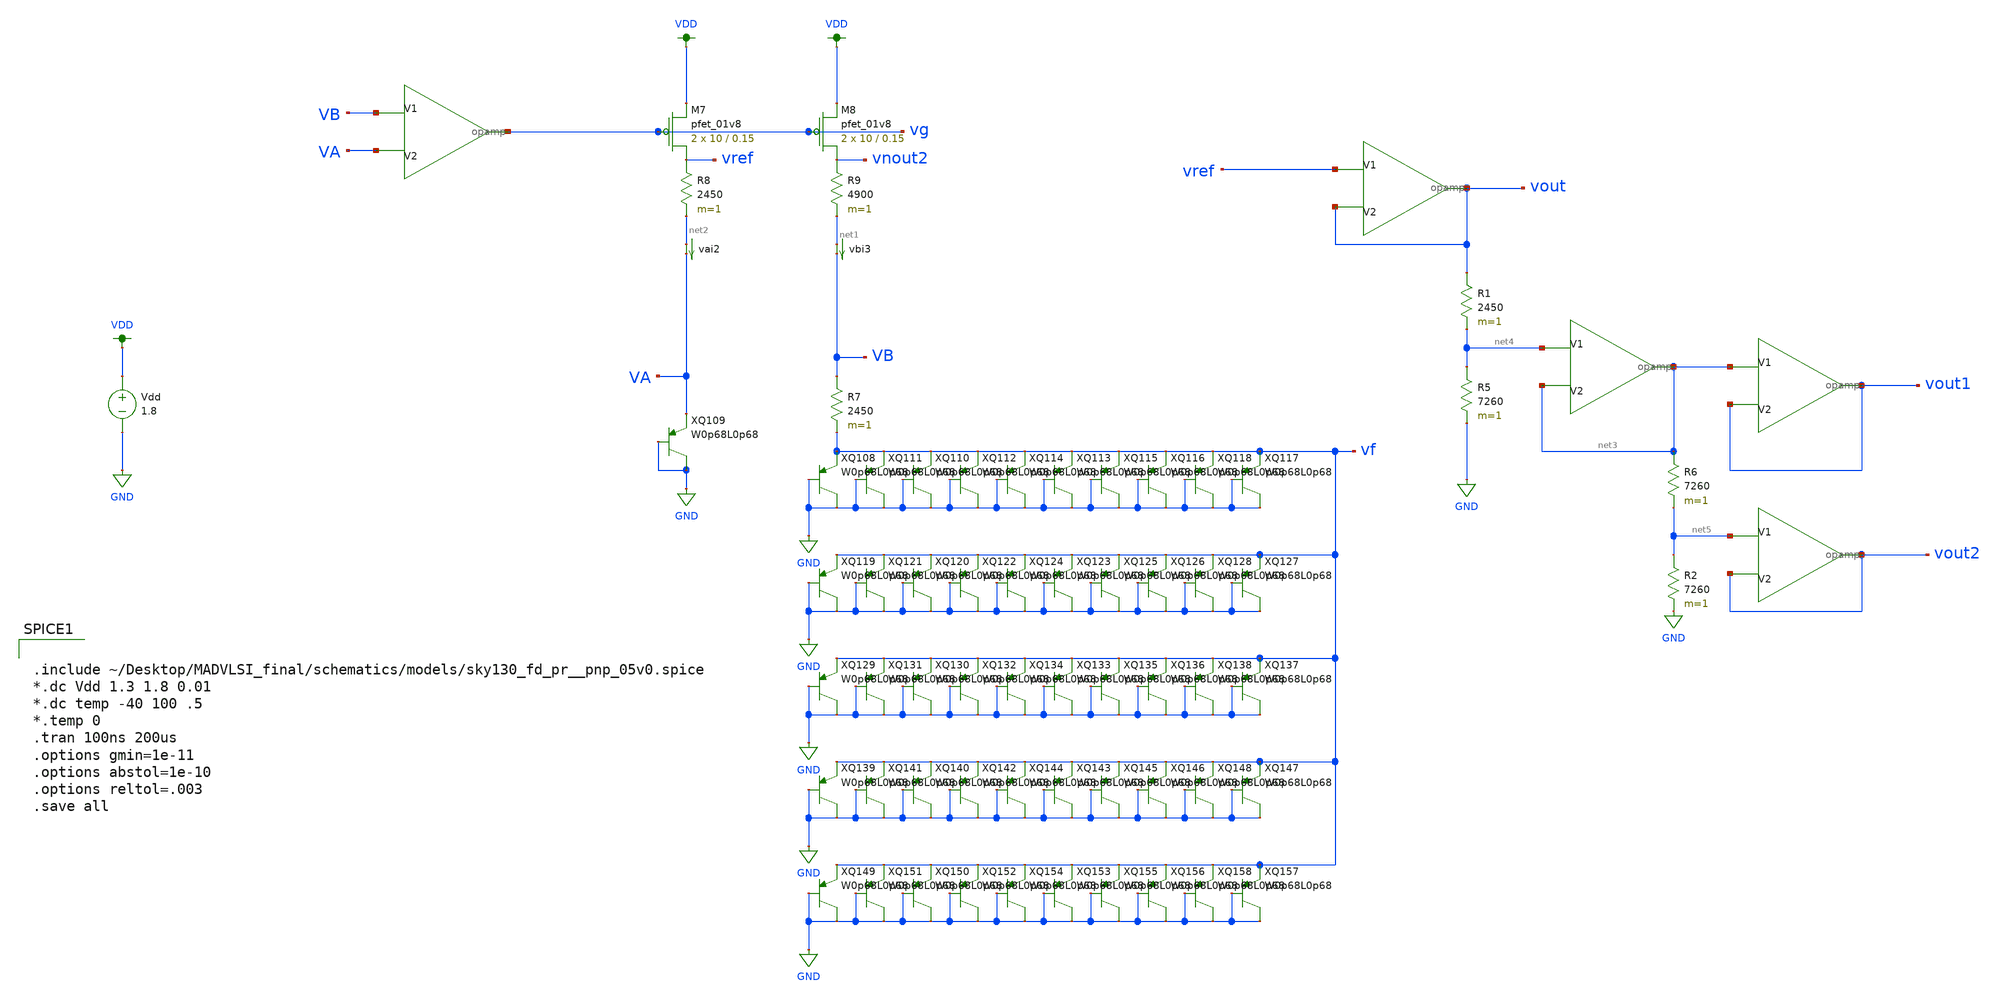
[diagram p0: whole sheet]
** sch_path: schematics/bandgap.sch
**.subckt bandgap
Vdd VDD GND 1.8
XM7 vref vg VDD VDD sky130_fd_pr__pfet_01v8 L=0.15 W=10 nf=1 ad='int((nf+1)/2) * W/nf * 0.29' as='int((nf+2)/2) * W/nf * 0.29'
+ pd='2*int((nf+1)/2) * (W/nf + 0.29)' ps='2*int((nf+2)/2) * (W/nf + 0.29)' nrd='0.29 / W' nrs='0.29 / W'
+ sa=0 sb=0 sd=0 mult=2 m=2
XQ108 vf GND GND sky130_fd_pr__pnp_05v0
XQ109 VA GND GND sky130_fd_pr__pnp_05v0
R7 VB vf 2450 m=1
XQ110 vf GND GND sky130_fd_pr__pnp_05v0
XQ111 vf GND GND sky130_fd_pr__pnp_05v0
XQ112 vf GND GND sky130_fd_pr__pnp_05v0
XQ113 vf GND GND sky130_fd_pr__pnp_05v0
XQ114 vf GND GND sky130_fd_pr__pnp_05v0
XQ115 vf GND GND sky130_fd_pr__pnp_05v0
XQ116 vf GND GND sky130_fd_pr__pnp_05v0
XQ117 vf GND GND sky130_fd_pr__pnp_05v0
XQ118 vf GND GND sky130_fd_pr__pnp_05v0
XQ119 vf GND GND sky130_fd_pr__pnp_05v0
XQ120 vf GND GND sky130_fd_pr__pnp_05v0
XQ121 vf GND GND sky130_fd_pr__pnp_05v0
XQ122 vf GND GND sky130_fd_pr__pnp_05v0
XQ123 vf GND GND sky130_fd_pr__pnp_05v0
XQ124 vf GND GND sky130_fd_pr__pnp_05v0
XQ125 vf GND GND sky130_fd_pr__pnp_05v0
XQ126 vf GND GND sky130_fd_pr__pnp_05v0
XQ127 vf GND GND sky130_fd_pr__pnp_05v0
XQ128 vf GND GND sky130_fd_pr__pnp_05v0
XQ129 vf GND GND sky130_fd_pr__pnp_05v0
XQ130 vf GND GND sky130_fd_pr__pnp_05v0
XQ131 vf GND GND sky130_fd_pr__pnp_05v0
XQ132 vf GND GND sky130_fd_pr__pnp_05v0
XQ133 vf GND GND sky130_fd_pr__pnp_05v0
XQ134 vf GND GND sky130_fd_pr__pnp_05v0
XQ135 vf GND GND sky130_fd_pr__pnp_05v0
XQ136 vf GND GND sky130_fd_pr__pnp_05v0
XQ137 vf GND GND sky130_fd_pr__pnp_05v0
XQ138 vf GND GND sky130_fd_pr__pnp_05v0
XQ139 vf GND GND sky130_fd_pr__pnp_05v0
XQ140 vf GND GND sky130_fd_pr__pnp_05v0
XQ141 vf GND GND sky130_fd_pr__pnp_05v0
XQ142 vf GND GND sky130_fd_pr__pnp_05v0
XQ143 vf GND GND sky130_fd_pr__pnp_05v0
XQ144 vf GND GND sky130_fd_pr__pnp_05v0
XQ145 vf GND GND sky130_fd_pr__pnp_05v0
XQ146 vf GND GND sky130_fd_pr__pnp_05v0
XQ147 vf GND GND sky130_fd_pr__pnp_05v0
XQ148 vf GND GND sky130_fd_pr__pnp_05v0
XQ149 vf GND GND sky130_fd_pr__pnp_05v0
XQ150 vf GND GND sky130_fd_pr__pnp_05v0
XQ151 vf GND GND sky130_fd_pr__pnp_05v0
XQ152 vf GND GND sky130_fd_pr__pnp_05v0
XQ153 vf GND GND sky130_fd_pr__pnp_05v0
XQ154 vf GND GND sky130_fd_pr__pnp_05v0
XQ155 vf GND GND sky130_fd_pr__pnp_05v0
XQ156 vf GND GND sky130_fd_pr__pnp_05v0
XQ157 vf GND GND sky130_fd_pr__pnp_05v0
XQ158 vf GND GND sky130_fd_pr__pnp_05v0
vai2 net2 VA 0
.save i(vai2)
vbi3 net1 VB 0
.save i(vbi3)
X159 VB VA vg opamp
R8 vref net2 2450 m=1
R9 vnout2 net1 4900 m=1
XM8 vnout2 vg VDD VDD sky130_fd_pr__pfet_01v8 L=0.15 W=10 nf=1 ad='int((nf+1)/2) * W/nf * 0.29' as='int((nf+2)/2) * W/nf * 0.29'
+ pd='2*int((nf+1)/2) * (W/nf + 0.29)' ps='2*int((nf+2)/2) * (W/nf + 0.29)' nrd='0.29 / W' nrs='0.29 / W'
+ sa=0 sb=0 sd=0 mult=2 m=2
X2 vref vout vout opamp
R1 vout net4 2450 m=1
R5 net4 GND 7260 m=1
X3 net4 net3 net3 opamp
R6 net3 net5 7260 m=1
R2 net5 GND 7260 m=1
X4 net5 vout2 vout2 opamp
X5 net3 vout1 vout1 opamp
**** begin user architecture code

.option wnflag=1
.param MC_SWITCH=0.0
.lib ~/skywater/skywater-pdk/libraries/sky130_fd_pr_ngspice/latest/models/sky130.lib.spice tt



.include ~/Desktop/MADVLSI_final/schematics/models/sky130_fd_pr__pnp_05v0.spice
*.dc Vdd 1.3 1.8 0.01
*.dc temp -40 100 .5
*.temp 0
.tran 100ns 200us
.options gmin=1e-11
.options abstol=1e-10
.options reltol=.003
.save all


**** end user architecture code
**.ends

* expanding   symbol:  /home/madvlsi/Desktop/MADVLSI_final/schematics/opamp.sym # of pins=3
** sym_path: schematics/opamp.sym
** sch_path: schematics/opamp.sch
.subckt opamp V1 V2 VOUT
*.ipin V1
*.ipin V2
*.opin VOUT
XM19 net12 net10 GND VDD sky130_fd_pr__pfet_01v8 L=.6 W=1.5 nf=1 ad='int((nf+1)/2) * W/nf * 0.29' as='int((nf+2)/2) * W/nf * 0.29'
+ pd='2*int((nf+1)/2) * (W/nf + 0.29)' ps='2*int((nf+2)/2) * (W/nf + 0.29)' nrd='0.29 / W' nrs='0.29 / W'
+ sa=0 sb=0 sd=0 mult=1 m=1
XMD20 VDD VDD net12 VDD sky130_fd_pr__pfet_01v8 L=.6 W=1.5 nf=1 ad='int((nf+1)/2) * W/nf * 0.29' as='int((nf+2)/2) * W/nf * 0.29'
+ pd='2*int((nf+1)/2) * (W/nf + 0.29)' ps='2*int((nf+2)/2) * (W/nf + 0.29)' nrd='0.29 / W' nrs='0.29 / W'
+ sa=0 sb=0 sd=0 mult=1 m=1
XM22 net12 net10 net9 VDD sky130_fd_pr__pfet_01v8 L=.6 W=1.5 nf=1 ad='int((nf+1)/2) * W/nf * 0.29' as='int((nf+2)/2) * W/nf * 0.29'
+ pd='2*int((nf+1)/2) * (W/nf + 0.29)' ps='2*int((nf+2)/2) * (W/nf + 0.29)' nrd='0.29 / W' nrs='0.29 / W'
+ sa=0 sb=0 sd=0 mult=1 m=1
XM23 GND net10 net12 VDD sky130_fd_pr__pfet_01v8 L=.6 W=1.5 nf=1 ad='int((nf+1)/2) * W/nf * 0.29' as='int((nf+2)/2) * W/nf * 0.29'
+ pd='2*int((nf+1)/2) * (W/nf + 0.29)' ps='2*int((nf+2)/2) * (W/nf + 0.29)' nrd='0.29 / W' nrs='0.29 / W'
+ sa=0 sb=0 sd=0 mult=1 m=1
XMD24 net9 VDD net10 VDD sky130_fd_pr__pfet_01v8 L=.6 W=1.5 nf=1 ad='int((nf+1)/2) * W/nf * 0.29' as='int((nf+2)/2) * W/nf * 0.29'
+ pd='2*int((nf+1)/2) * (W/nf + 0.29)' ps='2*int((nf+2)/2) * (W/nf + 0.29)' nrd='0.29 / W' nrs='0.29 / W'
+ sa=0 sb=0 sd=0 mult=1 m=1
XM25 VDD net10 net12 VDD sky130_fd_pr__pfet_01v8 L=.6 W=1.5 nf=1 ad='int((nf+1)/2) * W/nf * 0.29' as='int((nf+2)/2) * W/nf * 0.29'
+ pd='2*int((nf+1)/2) * (W/nf + 0.29)' ps='2*int((nf+2)/2) * (W/nf + 0.29)' nrd='0.29 / W' nrs='0.29 / W'
+ sa=0 sb=0 sd=0 mult=1 m=1
XM26 net7 V2 net11 VDD sky130_fd_pr__pfet_01v8 L=.6 W=1.5 nf=1 ad='int((nf+1)/2) * W/nf * 0.29' as='int((nf+2)/2) * W/nf * 0.29'
+ pd='2*int((nf+1)/2) * (W/nf + 0.29)' ps='2*int((nf+2)/2) * (W/nf + 0.29)' nrd='0.29 / W' nrs='0.29 / W'
+ sa=0 sb=0 sd=0 mult=1 m=1
XMD27 net5 VDD net14 VDD sky130_fd_pr__pfet_01v8 L=.6 W=1.5 nf=1 ad='int((nf+1)/2) * W/nf * 0.29' as='int((nf+2)/2) * W/nf * 0.29'
+ pd='2*int((nf+1)/2) * (W/nf + 0.29)' ps='2*int((nf+2)/2) * (W/nf + 0.29)' nrd='0.29 / W' nrs='0.29 / W'
+ sa=0 sb=0 sd=0 mult=1 m=1
XM28 net6 V1 net11 VDD sky130_fd_pr__pfet_01v8 L=.6 W=1.5 nf=1 ad='int((nf+1)/2) * W/nf * 0.29' as='int((nf+2)/2) * W/nf * 0.29'
+ pd='2*int((nf+1)/2) * (W/nf + 0.29)' ps='2*int((nf+2)/2) * (W/nf + 0.29)' nrd='0.29 / W' nrs='0.29 / W'
+ sa=0 sb=0 sd=0 mult=1 m=1
XM29 net11 net10 VDD VDD sky130_fd_pr__pfet_01v8 L=.6 W=1.5 nf=1 ad='int((nf+1)/2) * W/nf * 0.29' as='int((nf+2)/2) * W/nf * 0.29'
+ pd='2*int((nf+1)/2) * (W/nf + 0.29)' ps='2*int((nf+2)/2) * (W/nf + 0.29)' nrd='0.29 / W' nrs='0.29 / W'
+ sa=0 sb=0 sd=0 mult=1 m=1
XMD30 net11 VDD VDD VDD sky130_fd_pr__pfet_01v8 L=.6 W=1.5 nf=1 ad='int((nf+1)/2) * W/nf * 0.29' as='int((nf+2)/2) * W/nf * 0.29'
+ pd='2*int((nf+1)/2) * (W/nf + 0.29)' ps='2*int((nf+2)/2) * (W/nf + 0.29)' nrd='0.29 / W' nrs='0.29 / W'
+ sa=0 sb=0 sd=0 mult=1 m=1
XMD31 net2 VDD net13 VDD sky130_fd_pr__pfet_01v8 L=.6 W=1.5 nf=1 ad='int((nf+1)/2) * W/nf * 0.29' as='int((nf+2)/2) * W/nf * 0.29'
+ pd='2*int((nf+1)/2) * (W/nf + 0.29)' ps='2*int((nf+2)/2) * (W/nf + 0.29)' nrd='0.29 / W' nrs='0.29 / W'
+ sa=0 sb=0 sd=0 mult=1 m=1
XM32 net4 net5 net5 VDD sky130_fd_pr__pfet_01v8 L=.6 W=1.5 nf=1 ad='int((nf+1)/2) * W/nf * 0.29' as='int((nf+2)/2) * W/nf * 0.29'
+ pd='2*int((nf+1)/2) * (W/nf + 0.29)' ps='2*int((nf+2)/2) * (W/nf + 0.29)' nrd='0.29 / W' nrs='0.29 / W'
+ sa=0 sb=0 sd=0 mult=1 m=1
XM33 VDD net10 net4 VDD sky130_fd_pr__pfet_01v8 L=.6 W=1.5 nf=1 ad='int((nf+1)/2) * W/nf * 0.29' as='int((nf+2)/2) * W/nf * 0.29'
+ pd='2*int((nf+1)/2) * (W/nf + 0.29)' ps='2*int((nf+2)/2) * (W/nf + 0.29)' nrd='0.29 / W' nrs='0.29 / W'
+ sa=0 sb=0 sd=0 mult=1 m=1
XM34 net3 net5 net2 VDD sky130_fd_pr__pfet_01v8 L=.6 W=1.5 nf=1 ad='int((nf+1)/2) * W/nf * 0.29' as='int((nf+2)/2) * W/nf * 0.29'
+ pd='2*int((nf+1)/2) * (W/nf + 0.29)' ps='2*int((nf+2)/2) * (W/nf + 0.29)' nrd='0.29 / W' nrs='0.29 / W'
+ sa=0 sb=0 sd=0 mult=1 m=1
XM35 VDD net10 net3 VDD sky130_fd_pr__pfet_01v8 L=.6 W=1.5 nf=1 ad='int((nf+1)/2) * W/nf * 0.29' as='int((nf+2)/2) * W/nf * 0.29'
+ pd='2*int((nf+1)/2) * (W/nf + 0.29)' ps='2*int((nf+2)/2) * (W/nf + 0.29)' nrd='0.29 / W' nrs='0.29 / W'
+ sa=0 sb=0 sd=0 mult=1 m=1
XM36 VOUT net2 VDD VDD sky130_fd_pr__pfet_01v8 L=.6 W=1.5 nf=1 ad='int((nf+1)/2) * W/nf * 0.29' as='int((nf+2)/2) * W/nf * 0.29'
+ pd='2*int((nf+1)/2) * (W/nf + 0.29)' ps='2*int((nf+2)/2) * (W/nf + 0.29)' nrd='0.29 / W' nrs='0.29 / W'
+ sa=0 sb=0 sd=0 mult=1 m=1
XM37 VDD net2 VOUT VDD sky130_fd_pr__pfet_01v8 L=.6 W=1.5 nf=1 ad='int((nf+1)/2) * W/nf * 0.29' as='int((nf+2)/2) * W/nf * 0.29'
+ pd='2*int((nf+1)/2) * (W/nf + 0.29)' ps='2*int((nf+2)/2) * (W/nf + 0.29)' nrd='0.29 / W' nrs='0.29 / W'
+ sa=0 sb=0 sd=0 mult=1 m=1
XM38 VOUT net2 VDD VDD sky130_fd_pr__pfet_01v8 L=.6 W=1.5 nf=1 ad='int((nf+1)/2) * W/nf * 0.29' as='int((nf+2)/2) * W/nf * 0.29'
+ pd='2*int((nf+1)/2) * (W/nf + 0.29)' ps='2*int((nf+2)/2) * (W/nf + 0.29)' nrd='0.29 / W' nrs='0.29 / W'
+ sa=0 sb=0 sd=0 mult=1 m=1
XM39 VDD net2 VOUT VDD sky130_fd_pr__pfet_01v8 L=.6 W=1.5 nf=1 ad='int((nf+1)/2) * W/nf * 0.29' as='int((nf+2)/2) * W/nf * 0.29'
+ pd='2*int((nf+1)/2) * (W/nf + 0.29)' ps='2*int((nf+2)/2) * (W/nf + 0.29)' nrd='0.29 / W' nrs='0.29 / W'
+ sa=0 sb=0 sd=0 mult=1 m=1
XM40 net1 net9 VDD GND sky130_fd_pr__nfet_01v8 L=.6 W=1.5 nf=1 ad='int((nf+1)/2) * W/nf * 0.29' as='int((nf+2)/2) * W/nf * 0.29'
+ pd='2*int((nf+1)/2) * (W/nf + 0.29)' ps='2*int((nf+2)/2) * (W/nf + 0.29)' nrd='0.29 / W' nrs='0.29 / W'
+ sa=0 sb=0 sd=0 mult=1 m=1
XMD41 GND GND net1 GND sky130_fd_pr__nfet_01v8 L=.6 W=1.5 nf=1 ad='int((nf+1)/2) * W/nf * 0.29' as='int((nf+2)/2) * W/nf * 0.29'
+ pd='2*int((nf+1)/2) * (W/nf + 0.29)' ps='2*int((nf+2)/2) * (W/nf + 0.29)' nrd='0.29 / W' nrs='0.29 / W'
+ sa=0 sb=0 sd=0 mult=1 m=1
XM42 net1 net9 net10 GND sky130_fd_pr__nfet_01v8 L=.6 W=1.5 nf=1 ad='int((nf+1)/2) * W/nf * 0.29' as='int((nf+2)/2) * W/nf * 0.29'
+ pd='2*int((nf+1)/2) * (W/nf + 0.29)' ps='2*int((nf+2)/2) * (W/nf + 0.29)' nrd='0.29 / W' nrs='0.29 / W'
+ sa=0 sb=0 sd=0 mult=1 m=1
XM43 VDD net9 net1 GND sky130_fd_pr__nfet_01v8 L=.6 W=1.5 nf=1 ad='int((nf+1)/2) * W/nf * 0.29' as='int((nf+2)/2) * W/nf * 0.29'
+ pd='2*int((nf+1)/2) * (W/nf + 0.29)' ps='2*int((nf+2)/2) * (W/nf + 0.29)' nrd='0.29 / W' nrs='0.29 / W'
+ sa=0 sb=0 sd=0 mult=1 m=1
XMD44 net10 GND net9 GND sky130_fd_pr__nfet_01v8 L=.6 W=1.5 nf=1 ad='int((nf+1)/2) * W/nf * 0.29' as='int((nf+2)/2) * W/nf * 0.29'
+ pd='2*int((nf+1)/2) * (W/nf + 0.29)' ps='2*int((nf+2)/2) * (W/nf + 0.29)' nrd='0.29 / W' nrs='0.29 / W'
+ sa=0 sb=0 sd=0 mult=1 m=1
XM45 GND net9 net1 GND sky130_fd_pr__nfet_01v8 L=.6 W=1.5 nf=1 ad='int((nf+1)/2) * W/nf * 0.29' as='int((nf+2)/2) * W/nf * 0.29'
+ pd='2*int((nf+1)/2) * (W/nf + 0.29)' ps='2*int((nf+2)/2) * (W/nf + 0.29)' nrd='0.29 / W' nrs='0.29 / W'
+ sa=0 sb=0 sd=0 mult=1 m=1
XM46 net3 V1 net8 GND sky130_fd_pr__nfet_01v8 L=.6 W=1.5 nf=1 ad='int((nf+1)/2) * W/nf * 0.29' as='int((nf+2)/2) * W/nf * 0.29'
+ pd='2*int((nf+1)/2) * (W/nf + 0.29)' ps='2*int((nf+2)/2) * (W/nf + 0.29)' nrd='0.29 / W' nrs='0.29 / W'
+ sa=0 sb=0 sd=0 mult=1 m=1
XMD47 net5 GND net15 GND sky130_fd_pr__nfet_01v8 L=.6 W=1.5 nf=1 ad='int((nf+1)/2) * W/nf * 0.29' as='int((nf+2)/2) * W/nf * 0.29'
+ pd='2*int((nf+1)/2) * (W/nf + 0.29)' ps='2*int((nf+2)/2) * (W/nf + 0.29)' nrd='0.29 / W' nrs='0.29 / W'
+ sa=0 sb=0 sd=0 mult=1 m=1
XM48 net4 V2 net8 GND sky130_fd_pr__nfet_01v8 L=.6 W=1.5 nf=1 ad='int((nf+1)/2) * W/nf * 0.29' as='int((nf+2)/2) * W/nf * 0.29'
+ pd='2*int((nf+1)/2) * (W/nf + 0.29)' ps='2*int((nf+2)/2) * (W/nf + 0.29)' nrd='0.29 / W' nrs='0.29 / W'
+ sa=0 sb=0 sd=0 mult=1 m=1
XM49 net8 net9 GND GND sky130_fd_pr__nfet_01v8 L=.6 W=1.5 nf=1 ad='int((nf+1)/2) * W/nf * 0.29' as='int((nf+2)/2) * W/nf * 0.29'
+ pd='2*int((nf+1)/2) * (W/nf + 0.29)' ps='2*int((nf+2)/2) * (W/nf + 0.29)' nrd='0.29 / W' nrs='0.29 / W'
+ sa=0 sb=0 sd=0 mult=1 m=1
XMD50 net8 GND GND GND sky130_fd_pr__nfet_01v8 L=.6 W=1.5 nf=1 ad='int((nf+1)/2) * W/nf * 0.29' as='int((nf+2)/2) * W/nf * 0.29'
+ pd='2*int((nf+1)/2) * (W/nf + 0.29)' ps='2*int((nf+2)/2) * (W/nf + 0.29)' nrd='0.29 / W' nrs='0.29 / W'
+ sa=0 sb=0 sd=0 mult=1 m=1
XMD51 net2 GND net16 GND sky130_fd_pr__nfet_01v8 L=.6 W=1.5 nf=1 ad='int((nf+1)/2) * W/nf * 0.29' as='int((nf+2)/2) * W/nf * 0.29'
+ pd='2*int((nf+1)/2) * (W/nf + 0.29)' ps='2*int((nf+2)/2) * (W/nf + 0.29)' nrd='0.29 / W' nrs='0.29 / W'
+ sa=0 sb=0 sd=0 mult=1 m=1
XM52 GND net9 net7 GND sky130_fd_pr__nfet_01v8 L=.6 W=1.5 nf=1 ad='int((nf+1)/2) * W/nf * 0.29' as='int((nf+2)/2) * W/nf * 0.29'
+ pd='2*int((nf+1)/2) * (W/nf + 0.29)' ps='2*int((nf+2)/2) * (W/nf + 0.29)' nrd='0.29 / W' nrs='0.29 / W'
+ sa=0 sb=0 sd=0 mult=1 m=1
XMD53 VOUT GND GND GND sky130_fd_pr__nfet_01v8 L=.6 W=1.5 nf=1 ad='int((nf+1)/2) * W/nf * 0.29' as='int((nf+2)/2) * W/nf * 0.29'
+ pd='2*int((nf+1)/2) * (W/nf + 0.29)' ps='2*int((nf+2)/2) * (W/nf + 0.29)' nrd='0.29 / W' nrs='0.29 / W'
+ sa=0 sb=0 sd=0 mult=1 m=1
XM54 GND net9 net6 GND sky130_fd_pr__nfet_01v8 L=.6 W=1.5 nf=1 ad='int((nf+1)/2) * W/nf * 0.29' as='int((nf+2)/2) * W/nf * 0.29'
+ pd='2*int((nf+1)/2) * (W/nf + 0.29)' ps='2*int((nf+2)/2) * (W/nf + 0.29)' nrd='0.29 / W' nrs='0.29 / W'
+ sa=0 sb=0 sd=0 mult=1 m=1
XM55 net7 net5 net5 GND sky130_fd_pr__nfet_01v8 L=.6 W=1.5 nf=1 ad='int((nf+1)/2) * W/nf * 0.29' as='int((nf+2)/2) * W/nf * 0.29'
+ pd='2*int((nf+1)/2) * (W/nf + 0.29)' ps='2*int((nf+2)/2) * (W/nf + 0.29)' nrd='0.29 / W' nrs='0.29 / W'
+ sa=0 sb=0 sd=0 mult=1 m=1
XM56 net6 net5 net2 GND sky130_fd_pr__nfet_01v8 L=.6 W=1.5 nf=1 ad='int((nf+1)/2) * W/nf * 0.29' as='int((nf+2)/2) * W/nf * 0.29'
+ pd='2*int((nf+1)/2) * (W/nf + 0.29)' ps='2*int((nf+2)/2) * (W/nf + 0.29)' nrd='0.29 / W' nrs='0.29 / W'
+ sa=0 sb=0 sd=0 mult=1 m=1
XMD57 VOUT GND GND GND sky130_fd_pr__nfet_01v8 L=.6 W=1.5 nf=1 ad='int((nf+1)/2) * W/nf * 0.29' as='int((nf+2)/2) * W/nf * 0.29'
+ pd='2*int((nf+1)/2) * (W/nf + 0.29)' ps='2*int((nf+2)/2) * (W/nf + 0.29)' nrd='0.29 / W' nrs='0.29 / W'
+ sa=0 sb=0 sd=0 mult=1 m=1
XM58 GND net2 VOUT GND sky130_fd_pr__nfet_01v8 L=.6 W=1.5 nf=1 ad='int((nf+1)/2) * W/nf * 0.29' as='int((nf+2)/2) * W/nf * 0.29'
+ pd='2*int((nf+1)/2) * (W/nf + 0.29)' ps='2*int((nf+2)/2) * (W/nf + 0.29)' nrd='0.29 / W' nrs='0.29 / W'
+ sa=0 sb=0 sd=0 mult=1 m=1
XM59 GND net2 VOUT GND sky130_fd_pr__nfet_01v8 L=.6 W=1.5 nf=1 ad='int((nf+1)/2) * W/nf * 0.29' as='int((nf+2)/2) * W/nf * 0.29'
+ pd='2*int((nf+1)/2) * (W/nf + 0.29)' ps='2*int((nf+2)/2) * (W/nf + 0.29)' nrd='0.29 / W' nrs='0.29 / W'
+ sa=0 sb=0 sd=0 mult=1 m=1
XM60 net12 net10 GND VDD sky130_fd_pr__pfet_01v8 L=.6 W=1.5 nf=1 ad='int((nf+1)/2) * W/nf * 0.29' as='int((nf+2)/2) * W/nf * 0.29'
+ pd='2*int((nf+1)/2) * (W/nf + 0.29)' ps='2*int((nf+2)/2) * (W/nf + 0.29)' nrd='0.29 / W' nrs='0.29 / W'
+ sa=0 sb=0 sd=0 mult=1 m=1
XM61 net10 net10 net4 VDD sky130_fd_pr__pfet_01v8 L=.6 W=1.5 nf=1 ad='int((nf+1)/2) * W/nf * 0.29' as='int((nf+2)/2) * W/nf * 0.29'
+ pd='2*int((nf+1)/2) * (W/nf + 0.29)' ps='2*int((nf+2)/2) * (W/nf + 0.29)' nrd='0.29 / W' nrs='0.29 / W'
+ sa=0 sb=0 sd=0 mult=1 m=1
XM62 net1 net9 VDD GND sky130_fd_pr__nfet_01v8 L=.6 W=1.5 nf=1 ad='int((nf+1)/2) * W/nf * 0.29' as='int((nf+2)/2) * W/nf * 0.29'
+ pd='2*int((nf+1)/2) * (W/nf + 0.29)' ps='2*int((nf+2)/2) * (W/nf + 0.29)' nrd='0.29 / W' nrs='0.29 / W'
+ sa=0 sb=0 sd=0 mult=1 m=1
XM63 net9 net9 net7 GND sky130_fd_pr__nfet_01v8 L=.6 W=1.5 nf=1 ad='int((nf+1)/2) * W/nf * 0.29' as='int((nf+2)/2) * W/nf * 0.29'
+ pd='2*int((nf+1)/2) * (W/nf + 0.29)' ps='2*int((nf+2)/2) * (W/nf + 0.29)' nrd='0.29 / W' nrs='0.29 / W'
+ sa=0 sb=0 sd=0 mult=1 m=1
XMD64 VDD GND GND GND sky130_fd_pr__nfet_01v8 L=.6 W=1.5 nf=1 ad='int((nf+1)/2) * W/nf * 0.29' as='int((nf+2)/2) * W/nf * 0.29'
+ pd='2*int((nf+1)/2) * (W/nf + 0.29)' ps='2*int((nf+2)/2) * (W/nf + 0.29)' nrd='0.29 / W' nrs='0.29 / W'
+ sa=0 sb=0 sd=0 mult=1 m=1
XMD65 net7 GND GND GND sky130_fd_pr__nfet_01v8 L=.6 W=1.5 nf=1 ad='int((nf+1)/2) * W/nf * 0.29' as='int((nf+2)/2) * W/nf * 0.29'
+ pd='2*int((nf+1)/2) * (W/nf + 0.29)' ps='2*int((nf+2)/2) * (W/nf + 0.29)' nrd='0.29 / W' nrs='0.29 / W'
+ sa=0 sb=0 sd=0 mult=1 m=1
XMD66 GND VDD VDD VDD sky130_fd_pr__pfet_01v8 L=.6 W=1.5 nf=1 ad='int((nf+1)/2) * W/nf * 0.29' as='int((nf+2)/2) * W/nf * 0.29'
+ pd='2*int((nf+1)/2) * (W/nf + 0.29)' ps='2*int((nf+2)/2) * (W/nf + 0.29)' nrd='0.29 / W' nrs='0.29 / W'
+ sa=0 sb=0 sd=0 mult=1 m=1
XMD67 net4 VDD VDD VDD sky130_fd_pr__pfet_01v8 L=.6 W=1.5 nf=1 ad='int((nf+1)/2) * W/nf * 0.29' as='int((nf+2)/2) * W/nf * 0.29'
+ pd='2*int((nf+1)/2) * (W/nf + 0.29)' ps='2*int((nf+2)/2) * (W/nf + 0.29)' nrd='0.29 / W' nrs='0.29 / W'
+ sa=0 sb=0 sd=0 mult=1 m=1
XMD1 net15 GND net3 GND sky130_fd_pr__nfet_01v8 L=.6 W=1.5 nf=1 ad='int((nf+1)/2) * W/nf * 0.29' as='int((nf+2)/2) * W/nf * 0.29'
+ pd='2*int((nf+1)/2) * (W/nf + 0.29)' ps='2*int((nf+2)/2) * (W/nf + 0.29)' nrd='0.29 / W' nrs='0.29 / W'
+ sa=0 sb=0 sd=0 mult=1 m=1
XMD2 net16 GND net4 GND sky130_fd_pr__nfet_01v8 L=.6 W=1.5 nf=1 ad='int((nf+1)/2) * W/nf * 0.29' as='int((nf+2)/2) * W/nf * 0.29'
+ pd='2*int((nf+1)/2) * (W/nf + 0.29)' ps='2*int((nf+2)/2) * (W/nf + 0.29)' nrd='0.29 / W' nrs='0.29 / W'
+ sa=0 sb=0 sd=0 mult=1 m=1
XMD3 net13 VDD net6 VDD sky130_fd_pr__pfet_01v8 L=.6 W=1.5 nf=1 ad='int((nf+1)/2) * W/nf * 0.29' as='int((nf+2)/2) * W/nf * 0.29'
+ pd='2*int((nf+1)/2) * (W/nf + 0.29)' ps='2*int((nf+2)/2) * (W/nf + 0.29)' nrd='0.29 / W' nrs='0.29 / W'
+ sa=0 sb=0 sd=0 mult=1 m=1
XMD4 net14 VDD net7 VDD sky130_fd_pr__pfet_01v8 L=.6 W=1.5 nf=1 ad='int((nf+1)/2) * W/nf * 0.29' as='int((nf+2)/2) * W/nf * 0.29'
+ pd='2*int((nf+1)/2) * (W/nf + 0.29)' ps='2*int((nf+2)/2) * (W/nf + 0.29)' nrd='0.29 / W' nrs='0.29 / W'
+ sa=0 sb=0 sd=0 mult=1 m=1
XM1 net21 net10 GND VDD sky130_fd_pr__pfet_01v8 L=.6 W=1.5 nf=1 ad='int((nf+1)/2) * W/nf * 0.29' as='int((nf+2)/2) * W/nf * 0.29'
+ pd='2*int((nf+1)/2) * (W/nf + 0.29)' ps='2*int((nf+2)/2) * (W/nf + 0.29)' nrd='0.29 / W' nrs='0.29 / W'
+ sa=0 sb=0 sd=0 mult=1 m=1
XMD5 VDD VDD net21 VDD sky130_fd_pr__pfet_01v8 L=.6 W=1.5 nf=1 ad='int((nf+1)/2) * W/nf * 0.29' as='int((nf+2)/2) * W/nf * 0.29'
+ pd='2*int((nf+1)/2) * (W/nf + 0.29)' ps='2*int((nf+2)/2) * (W/nf + 0.29)' nrd='0.29 / W' nrs='0.29 / W'
+ sa=0 sb=0 sd=0 mult=1 m=1
XM6 net21 net10 net9 VDD sky130_fd_pr__pfet_01v8 L=.6 W=1.5 nf=1 ad='int((nf+1)/2) * W/nf * 0.29' as='int((nf+2)/2) * W/nf * 0.29'
+ pd='2*int((nf+1)/2) * (W/nf + 0.29)' ps='2*int((nf+2)/2) * (W/nf + 0.29)' nrd='0.29 / W' nrs='0.29 / W'
+ sa=0 sb=0 sd=0 mult=1 m=1
XM7 GND net10 net21 VDD sky130_fd_pr__pfet_01v8 L=.6 W=1.5 nf=1 ad='int((nf+1)/2) * W/nf * 0.29' as='int((nf+2)/2) * W/nf * 0.29'
+ pd='2*int((nf+1)/2) * (W/nf + 0.29)' ps='2*int((nf+2)/2) * (W/nf + 0.29)' nrd='0.29 / W' nrs='0.29 / W'
+ sa=0 sb=0 sd=0 mult=1 m=1
XMD8 net9 VDD net10 VDD sky130_fd_pr__pfet_01v8 L=.6 W=1.5 nf=1 ad='int((nf+1)/2) * W/nf * 0.29' as='int((nf+2)/2) * W/nf * 0.29'
+ pd='2*int((nf+1)/2) * (W/nf + 0.29)' ps='2*int((nf+2)/2) * (W/nf + 0.29)' nrd='0.29 / W' nrs='0.29 / W'
+ sa=0 sb=0 sd=0 mult=1 m=1
XM9 VDD net10 net21 VDD sky130_fd_pr__pfet_01v8 L=.6 W=1.5 nf=1 ad='int((nf+1)/2) * W/nf * 0.29' as='int((nf+2)/2) * W/nf * 0.29'
+ pd='2*int((nf+1)/2) * (W/nf + 0.29)' ps='2*int((nf+2)/2) * (W/nf + 0.29)' nrd='0.29 / W' nrs='0.29 / W'
+ sa=0 sb=0 sd=0 mult=1 m=1
XM10 net7 V2 net20 VDD sky130_fd_pr__pfet_01v8 L=.6 W=1.5 nf=1 ad='int((nf+1)/2) * W/nf * 0.29' as='int((nf+2)/2) * W/nf * 0.29'
+ pd='2*int((nf+1)/2) * (W/nf + 0.29)' ps='2*int((nf+2)/2) * (W/nf + 0.29)' nrd='0.29 / W' nrs='0.29 / W'
+ sa=0 sb=0 sd=0 mult=1 m=1
XMD11 net18 VDD net23 VDD sky130_fd_pr__pfet_01v8 L=.6 W=1.5 nf=1 ad='int((nf+1)/2) * W/nf * 0.29' as='int((nf+2)/2) * W/nf * 0.29'
+ pd='2*int((nf+1)/2) * (W/nf + 0.29)' ps='2*int((nf+2)/2) * (W/nf + 0.29)' nrd='0.29 / W' nrs='0.29 / W'
+ sa=0 sb=0 sd=0 mult=1 m=1
XM12 net6 V1 net20 VDD sky130_fd_pr__pfet_01v8 L=.6 W=1.5 nf=1 ad='int((nf+1)/2) * W/nf * 0.29' as='int((nf+2)/2) * W/nf * 0.29'
+ pd='2*int((nf+1)/2) * (W/nf + 0.29)' ps='2*int((nf+2)/2) * (W/nf + 0.29)' nrd='0.29 / W' nrs='0.29 / W'
+ sa=0 sb=0 sd=0 mult=1 m=1
XM13 net20 net10 VDD VDD sky130_fd_pr__pfet_01v8 L=.6 W=1.5 nf=1 ad='int((nf+1)/2) * W/nf * 0.29' as='int((nf+2)/2) * W/nf * 0.29'
+ pd='2*int((nf+1)/2) * (W/nf + 0.29)' ps='2*int((nf+2)/2) * (W/nf + 0.29)' nrd='0.29 / W' nrs='0.29 / W'
+ sa=0 sb=0 sd=0 mult=1 m=1
XMD14 net20 VDD VDD VDD sky130_fd_pr__pfet_01v8 L=.6 W=1.5 nf=1 ad='int((nf+1)/2) * W/nf * 0.29' as='int((nf+2)/2) * W/nf * 0.29'
+ pd='2*int((nf+1)/2) * (W/nf + 0.29)' ps='2*int((nf+2)/2) * (W/nf + 0.29)' nrd='0.29 / W' nrs='0.29 / W'
+ sa=0 sb=0 sd=0 mult=1 m=1
XMD15 net2 VDD net22 VDD sky130_fd_pr__pfet_01v8 L=.6 W=1.5 nf=1 ad='int((nf+1)/2) * W/nf * 0.29' as='int((nf+2)/2) * W/nf * 0.29'
+ pd='2*int((nf+1)/2) * (W/nf + 0.29)' ps='2*int((nf+2)/2) * (W/nf + 0.29)' nrd='0.29 / W' nrs='0.29 / W'
+ sa=0 sb=0 sd=0 mult=1 m=1
XM16 net4 net18 net18 VDD sky130_fd_pr__pfet_01v8 L=.6 W=1.5 nf=1 ad='int((nf+1)/2) * W/nf * 0.29' as='int((nf+2)/2) * W/nf * 0.29'
+ pd='2*int((nf+1)/2) * (W/nf + 0.29)' ps='2*int((nf+2)/2) * (W/nf + 0.29)' nrd='0.29 / W' nrs='0.29 / W'
+ sa=0 sb=0 sd=0 mult=1 m=1
XM17 VDD net10 net4 VDD sky130_fd_pr__pfet_01v8 L=.6 W=1.5 nf=1 ad='int((nf+1)/2) * W/nf * 0.29' as='int((nf+2)/2) * W/nf * 0.29'
+ pd='2*int((nf+1)/2) * (W/nf + 0.29)' ps='2*int((nf+2)/2) * (W/nf + 0.29)' nrd='0.29 / W' nrs='0.29 / W'
+ sa=0 sb=0 sd=0 mult=1 m=1
XM18 net3 net18 net2 VDD sky130_fd_pr__pfet_01v8 L=.6 W=1.5 nf=1 ad='int((nf+1)/2) * W/nf * 0.29' as='int((nf+2)/2) * W/nf * 0.29'
+ pd='2*int((nf+1)/2) * (W/nf + 0.29)' ps='2*int((nf+2)/2) * (W/nf + 0.29)' nrd='0.29 / W' nrs='0.29 / W'
+ sa=0 sb=0 sd=0 mult=1 m=1
XM20 VDD net10 net3 VDD sky130_fd_pr__pfet_01v8 L=.6 W=1.5 nf=1 ad='int((nf+1)/2) * W/nf * 0.29' as='int((nf+2)/2) * W/nf * 0.29'
+ pd='2*int((nf+1)/2) * (W/nf + 0.29)' ps='2*int((nf+2)/2) * (W/nf + 0.29)' nrd='0.29 / W' nrs='0.29 / W'
+ sa=0 sb=0 sd=0 mult=1 m=1
XM21 VOUT net2 VDD VDD sky130_fd_pr__pfet_01v8 L=.6 W=1.5 nf=1 ad='int((nf+1)/2) * W/nf * 0.29' as='int((nf+2)/2) * W/nf * 0.29'
+ pd='2*int((nf+1)/2) * (W/nf + 0.29)' ps='2*int((nf+2)/2) * (W/nf + 0.29)' nrd='0.29 / W' nrs='0.29 / W'
+ sa=0 sb=0 sd=0 mult=1 m=1
XM24 VDD net2 VOUT VDD sky130_fd_pr__pfet_01v8 L=.6 W=1.5 nf=1 ad='int((nf+1)/2) * W/nf * 0.29' as='int((nf+2)/2) * W/nf * 0.29'
+ pd='2*int((nf+1)/2) * (W/nf + 0.29)' ps='2*int((nf+2)/2) * (W/nf + 0.29)' nrd='0.29 / W' nrs='0.29 / W'
+ sa=0 sb=0 sd=0 mult=1 m=1
XM27 VOUT net2 VDD VDD sky130_fd_pr__pfet_01v8 L=.6 W=1.5 nf=1 ad='int((nf+1)/2) * W/nf * 0.29' as='int((nf+2)/2) * W/nf * 0.29'
+ pd='2*int((nf+1)/2) * (W/nf + 0.29)' ps='2*int((nf+2)/2) * (W/nf + 0.29)' nrd='0.29 / W' nrs='0.29 / W'
+ sa=0 sb=0 sd=0 mult=1 m=1
XM30 VDD net2 VOUT VDD sky130_fd_pr__pfet_01v8 L=.6 W=1.5 nf=1 ad='int((nf+1)/2) * W/nf * 0.29' as='int((nf+2)/2) * W/nf * 0.29'
+ pd='2*int((nf+1)/2) * (W/nf + 0.29)' ps='2*int((nf+2)/2) * (W/nf + 0.29)' nrd='0.29 / W' nrs='0.29 / W'
+ sa=0 sb=0 sd=0 mult=1 m=1
XM31 net17 net9 VDD GND sky130_fd_pr__nfet_01v8 L=.6 W=1.5 nf=1 ad='int((nf+1)/2) * W/nf * 0.29' as='int((nf+2)/2) * W/nf * 0.29'
+ pd='2*int((nf+1)/2) * (W/nf + 0.29)' ps='2*int((nf+2)/2) * (W/nf + 0.29)' nrd='0.29 / W' nrs='0.29 / W'
+ sa=0 sb=0 sd=0 mult=1 m=1
XMD32 GND GND net17 GND sky130_fd_pr__nfet_01v8 L=.6 W=1.5 nf=1 ad='int((nf+1)/2) * W/nf * 0.29' as='int((nf+2)/2) * W/nf * 0.29'
+ pd='2*int((nf+1)/2) * (W/nf + 0.29)' ps='2*int((nf+2)/2) * (W/nf + 0.29)' nrd='0.29 / W' nrs='0.29 / W'
+ sa=0 sb=0 sd=0 mult=1 m=1
XM41 net17 net9 net10 GND sky130_fd_pr__nfet_01v8 L=.6 W=1.5 nf=1 ad='int((nf+1)/2) * W/nf * 0.29' as='int((nf+2)/2) * W/nf * 0.29'
+ pd='2*int((nf+1)/2) * (W/nf + 0.29)' ps='2*int((nf+2)/2) * (W/nf + 0.29)' nrd='0.29 / W' nrs='0.29 / W'
+ sa=0 sb=0 sd=0 mult=1 m=1
XM44 VDD net9 net17 GND sky130_fd_pr__nfet_01v8 L=.6 W=1.5 nf=1 ad='int((nf+1)/2) * W/nf * 0.29' as='int((nf+2)/2) * W/nf * 0.29'
+ pd='2*int((nf+1)/2) * (W/nf + 0.29)' ps='2*int((nf+2)/2) * (W/nf + 0.29)' nrd='0.29 / W' nrs='0.29 / W'
+ sa=0 sb=0 sd=0 mult=1 m=1
XMD45 net10 GND net9 GND sky130_fd_pr__nfet_01v8 L=.6 W=1.5 nf=1 ad='int((nf+1)/2) * W/nf * 0.29' as='int((nf+2)/2) * W/nf * 0.29'
+ pd='2*int((nf+1)/2) * (W/nf + 0.29)' ps='2*int((nf+2)/2) * (W/nf + 0.29)' nrd='0.29 / W' nrs='0.29 / W'
+ sa=0 sb=0 sd=0 mult=1 m=1
XM47 GND net9 net17 GND sky130_fd_pr__nfet_01v8 L=.6 W=1.5 nf=1 ad='int((nf+1)/2) * W/nf * 0.29' as='int((nf+2)/2) * W/nf * 0.29'
+ pd='2*int((nf+1)/2) * (W/nf + 0.29)' ps='2*int((nf+2)/2) * (W/nf + 0.29)' nrd='0.29 / W' nrs='0.29 / W'
+ sa=0 sb=0 sd=0 mult=1 m=1
XM50 net3 V1 net19 GND sky130_fd_pr__nfet_01v8 L=.6 W=1.5 nf=1 ad='int((nf+1)/2) * W/nf * 0.29' as='int((nf+2)/2) * W/nf * 0.29'
+ pd='2*int((nf+1)/2) * (W/nf + 0.29)' ps='2*int((nf+2)/2) * (W/nf + 0.29)' nrd='0.29 / W' nrs='0.29 / W'
+ sa=0 sb=0 sd=0 mult=1 m=1
XMD52 net18 GND net24 GND sky130_fd_pr__nfet_01v8 L=.6 W=1.5 nf=1 ad='int((nf+1)/2) * W/nf * 0.29' as='int((nf+2)/2) * W/nf * 0.29'
+ pd='2*int((nf+1)/2) * (W/nf + 0.29)' ps='2*int((nf+2)/2) * (W/nf + 0.29)' nrd='0.29 / W' nrs='0.29 / W'
+ sa=0 sb=0 sd=0 mult=1 m=1
XM53 net4 V2 net19 GND sky130_fd_pr__nfet_01v8 L=.6 W=1.5 nf=1 ad='int((nf+1)/2) * W/nf * 0.29' as='int((nf+2)/2) * W/nf * 0.29'
+ pd='2*int((nf+1)/2) * (W/nf + 0.29)' ps='2*int((nf+2)/2) * (W/nf + 0.29)' nrd='0.29 / W' nrs='0.29 / W'
+ sa=0 sb=0 sd=0 mult=1 m=1
XM57 net19 net9 GND GND sky130_fd_pr__nfet_01v8 L=.6 W=1.5 nf=1 ad='int((nf+1)/2) * W/nf * 0.29' as='int((nf+2)/2) * W/nf * 0.29'
+ pd='2*int((nf+1)/2) * (W/nf + 0.29)' ps='2*int((nf+2)/2) * (W/nf + 0.29)' nrd='0.29 / W' nrs='0.29 / W'
+ sa=0 sb=0 sd=0 mult=1 m=1
XMD58 net19 GND GND GND sky130_fd_pr__nfet_01v8 L=.6 W=1.5 nf=1 ad='int((nf+1)/2) * W/nf * 0.29' as='int((nf+2)/2) * W/nf * 0.29'
+ pd='2*int((nf+1)/2) * (W/nf + 0.29)' ps='2*int((nf+2)/2) * (W/nf + 0.29)' nrd='0.29 / W' nrs='0.29 / W'
+ sa=0 sb=0 sd=0 mult=1 m=1
XMD59 net2 GND net25 GND sky130_fd_pr__nfet_01v8 L=.6 W=1.5 nf=1 ad='int((nf+1)/2) * W/nf * 0.29' as='int((nf+2)/2) * W/nf * 0.29'
+ pd='2*int((nf+1)/2) * (W/nf + 0.29)' ps='2*int((nf+2)/2) * (W/nf + 0.29)' nrd='0.29 / W' nrs='0.29 / W'
+ sa=0 sb=0 sd=0 mult=1 m=1
XM64 GND net9 net7 GND sky130_fd_pr__nfet_01v8 L=.6 W=1.5 nf=1 ad='int((nf+1)/2) * W/nf * 0.29' as='int((nf+2)/2) * W/nf * 0.29'
+ pd='2*int((nf+1)/2) * (W/nf + 0.29)' ps='2*int((nf+2)/2) * (W/nf + 0.29)' nrd='0.29 / W' nrs='0.29 / W'
+ sa=0 sb=0 sd=0 mult=1 m=1
XMD68 VOUT GND GND GND sky130_fd_pr__nfet_01v8 L=.6 W=1.5 nf=1 ad='int((nf+1)/2) * W/nf * 0.29' as='int((nf+2)/2) * W/nf * 0.29'
+ pd='2*int((nf+1)/2) * (W/nf + 0.29)' ps='2*int((nf+2)/2) * (W/nf + 0.29)' nrd='0.29 / W' nrs='0.29 / W'
+ sa=0 sb=0 sd=0 mult=1 m=1
XM69 GND net9 net6 GND sky130_fd_pr__nfet_01v8 L=.6 W=1.5 nf=1 ad='int((nf+1)/2) * W/nf * 0.29' as='int((nf+2)/2) * W/nf * 0.29'
+ pd='2*int((nf+1)/2) * (W/nf + 0.29)' ps='2*int((nf+2)/2) * (W/nf + 0.29)' nrd='0.29 / W' nrs='0.29 / W'
+ sa=0 sb=0 sd=0 mult=1 m=1
XM70 net7 net18 net18 GND sky130_fd_pr__nfet_01v8 L=.6 W=1.5 nf=1 ad='int((nf+1)/2) * W/nf * 0.29' as='int((nf+2)/2) * W/nf * 0.29'
+ pd='2*int((nf+1)/2) * (W/nf + 0.29)' ps='2*int((nf+2)/2) * (W/nf + 0.29)' nrd='0.29 / W' nrs='0.29 / W'
+ sa=0 sb=0 sd=0 mult=1 m=1
XM71 net6 net18 net2 GND sky130_fd_pr__nfet_01v8 L=.6 W=1.5 nf=1 ad='int((nf+1)/2) * W/nf * 0.29' as='int((nf+2)/2) * W/nf * 0.29'
+ pd='2*int((nf+1)/2) * (W/nf + 0.29)' ps='2*int((nf+2)/2) * (W/nf + 0.29)' nrd='0.29 / W' nrs='0.29 / W'
+ sa=0 sb=0 sd=0 mult=1 m=1
XMD72 VOUT GND GND GND sky130_fd_pr__nfet_01v8 L=.6 W=1.5 nf=1 ad='int((nf+1)/2) * W/nf * 0.29' as='int((nf+2)/2) * W/nf * 0.29'
+ pd='2*int((nf+1)/2) * (W/nf + 0.29)' ps='2*int((nf+2)/2) * (W/nf + 0.29)' nrd='0.29 / W' nrs='0.29 / W'
+ sa=0 sb=0 sd=0 mult=1 m=1
XM73 GND net2 VOUT GND sky130_fd_pr__nfet_01v8 L=.6 W=1.5 nf=1 ad='int((nf+1)/2) * W/nf * 0.29' as='int((nf+2)/2) * W/nf * 0.29'
+ pd='2*int((nf+1)/2) * (W/nf + 0.29)' ps='2*int((nf+2)/2) * (W/nf + 0.29)' nrd='0.29 / W' nrs='0.29 / W'
+ sa=0 sb=0 sd=0 mult=1 m=1
XM74 GND net2 VOUT GND sky130_fd_pr__nfet_01v8 L=.6 W=1.5 nf=1 ad='int((nf+1)/2) * W/nf * 0.29' as='int((nf+2)/2) * W/nf * 0.29'
+ pd='2*int((nf+1)/2) * (W/nf + 0.29)' ps='2*int((nf+2)/2) * (W/nf + 0.29)' nrd='0.29 / W' nrs='0.29 / W'
+ sa=0 sb=0 sd=0 mult=1 m=1
XM75 net21 net10 GND VDD sky130_fd_pr__pfet_01v8 L=.6 W=1.5 nf=1 ad='int((nf+1)/2) * W/nf * 0.29' as='int((nf+2)/2) * W/nf * 0.29'
+ pd='2*int((nf+1)/2) * (W/nf + 0.29)' ps='2*int((nf+2)/2) * (W/nf + 0.29)' nrd='0.29 / W' nrs='0.29 / W'
+ sa=0 sb=0 sd=0 mult=1 m=1
XM76 net10 net10 net4 VDD sky130_fd_pr__pfet_01v8 L=.6 W=1.5 nf=1 ad='int((nf+1)/2) * W/nf * 0.29' as='int((nf+2)/2) * W/nf * 0.29'
+ pd='2*int((nf+1)/2) * (W/nf + 0.29)' ps='2*int((nf+2)/2) * (W/nf + 0.29)' nrd='0.29 / W' nrs='0.29 / W'
+ sa=0 sb=0 sd=0 mult=1 m=1
XM77 net17 net9 VDD GND sky130_fd_pr__nfet_01v8 L=.6 W=1.5 nf=1 ad='int((nf+1)/2) * W/nf * 0.29' as='int((nf+2)/2) * W/nf * 0.29'
+ pd='2*int((nf+1)/2) * (W/nf + 0.29)' ps='2*int((nf+2)/2) * (W/nf + 0.29)' nrd='0.29 / W' nrs='0.29 / W'
+ sa=0 sb=0 sd=0 mult=1 m=1
XM78 net9 net9 net7 GND sky130_fd_pr__nfet_01v8 L=.6 W=1.5 nf=1 ad='int((nf+1)/2) * W/nf * 0.29' as='int((nf+2)/2) * W/nf * 0.29'
+ pd='2*int((nf+1)/2) * (W/nf + 0.29)' ps='2*int((nf+2)/2) * (W/nf + 0.29)' nrd='0.29 / W' nrs='0.29 / W'
+ sa=0 sb=0 sd=0 mult=1 m=1
XMD79 VDD GND GND GND sky130_fd_pr__nfet_01v8 L=.6 W=1.5 nf=1 ad='int((nf+1)/2) * W/nf * 0.29' as='int((nf+2)/2) * W/nf * 0.29'
+ pd='2*int((nf+1)/2) * (W/nf + 0.29)' ps='2*int((nf+2)/2) * (W/nf + 0.29)' nrd='0.29 / W' nrs='0.29 / W'
+ sa=0 sb=0 sd=0 mult=1 m=1
XMD80 net7 GND GND GND sky130_fd_pr__nfet_01v8 L=.6 W=1.5 nf=1 ad='int((nf+1)/2) * W/nf * 0.29' as='int((nf+2)/2) * W/nf * 0.29'
+ pd='2*int((nf+1)/2) * (W/nf + 0.29)' ps='2*int((nf+2)/2) * (W/nf + 0.29)' nrd='0.29 / W' nrs='0.29 / W'
+ sa=0 sb=0 sd=0 mult=1 m=1
XMD81 GND VDD VDD VDD sky130_fd_pr__pfet_01v8 L=.6 W=1.5 nf=1 ad='int((nf+1)/2) * W/nf * 0.29' as='int((nf+2)/2) * W/nf * 0.29'
+ pd='2*int((nf+1)/2) * (W/nf + 0.29)' ps='2*int((nf+2)/2) * (W/nf + 0.29)' nrd='0.29 / W' nrs='0.29 / W'
+ sa=0 sb=0 sd=0 mult=1 m=1
XMD82 net4 VDD VDD VDD sky130_fd_pr__pfet_01v8 L=.6 W=1.5 nf=1 ad='int((nf+1)/2) * W/nf * 0.29' as='int((nf+2)/2) * W/nf * 0.29'
+ pd='2*int((nf+1)/2) * (W/nf + 0.29)' ps='2*int((nf+2)/2) * (W/nf + 0.29)' nrd='0.29 / W' nrs='0.29 / W'
+ sa=0 sb=0 sd=0 mult=1 m=1
XMD83 net24 GND net3 GND sky130_fd_pr__nfet_01v8 L=.6 W=1.5 nf=1 ad='int((nf+1)/2) * W/nf * 0.29' as='int((nf+2)/2) * W/nf * 0.29'
+ pd='2*int((nf+1)/2) * (W/nf + 0.29)' ps='2*int((nf+2)/2) * (W/nf + 0.29)' nrd='0.29 / W' nrs='0.29 / W'
+ sa=0 sb=0 sd=0 mult=1 m=1
XMD84 net25 GND net4 GND sky130_fd_pr__nfet_01v8 L=.6 W=1.5 nf=1 ad='int((nf+1)/2) * W/nf * 0.29' as='int((nf+2)/2) * W/nf * 0.29'
+ pd='2*int((nf+1)/2) * (W/nf + 0.29)' ps='2*int((nf+2)/2) * (W/nf + 0.29)' nrd='0.29 / W' nrs='0.29 / W'
+ sa=0 sb=0 sd=0 mult=1 m=1
XMD85 net22 VDD net6 VDD sky130_fd_pr__pfet_01v8 L=.6 W=1.5 nf=1 ad='int((nf+1)/2) * W/nf * 0.29' as='int((nf+2)/2) * W/nf * 0.29'
+ pd='2*int((nf+1)/2) * (W/nf + 0.29)' ps='2*int((nf+2)/2) * (W/nf + 0.29)' nrd='0.29 / W' nrs='0.29 / W'
+ sa=0 sb=0 sd=0 mult=1 m=1
XMD86 net23 VDD net7 VDD sky130_fd_pr__pfet_01v8 L=.6 W=1.5 nf=1 ad='int((nf+1)/2) * W/nf * 0.29' as='int((nf+2)/2) * W/nf * 0.29'
+ pd='2*int((nf+1)/2) * (W/nf + 0.29)' ps='2*int((nf+2)/2) * (W/nf + 0.29)' nrd='0.29 / W' nrs='0.29 / W'
+ sa=0 sb=0 sd=0 mult=1 m=1
XC1 net2 VOUT sky130_fd_pr__cap_mim_m3_1 W=20 L=12 MF=1 m=1
.ends

.GLOBAL VDD
.GLOBAL GND
.end
